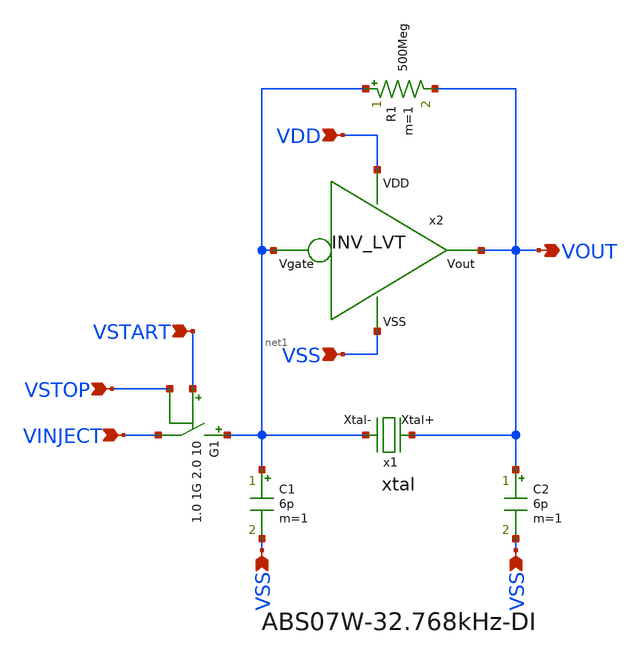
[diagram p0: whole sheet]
** sch_path: design/THESIS_EXP_RO_INVERTER_SKY130A/xtal_osc.sch
**.subckt xtal_osc VDD VSS VSS VSS VOUT VINJECT VSTOP VSTART
*.ipin VDD
*.ipin VSS
*.ipin VSS
*.ipin VSS
*.opin VOUT
*.ipin VINJECT
*.ipin VSTOP
*.ipin VSTART
x1 VOUT net1 xtal
x2 VDD net1 VOUT VSS INV_LVT
C1 net1 VSS 6p m=1
C2 VOUT VSS 6p m=1
R1 net1 VOUT 500Meg m=1
G1 net1 VINJECT vcr pwl(1) VSTART VSTOP 1.0 1G 2.0 10
**.ends
.end
